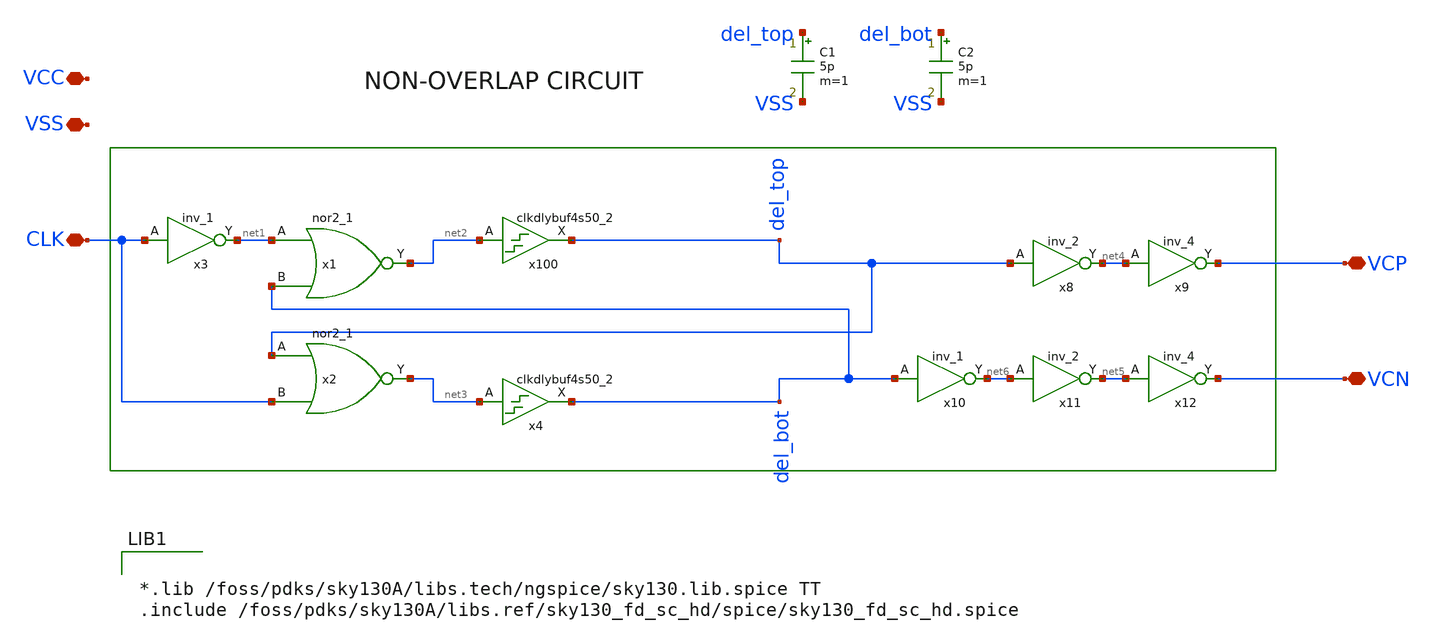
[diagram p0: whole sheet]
** sch_path: xschem/NOL_v3p1.sch
**.subckt NOL_v3p1 CLK VCP VCN VCC VSS
*.iopin CLK
*.iopin VCP
*.iopin VCN
*.iopin VCC
*.iopin VSS
x3 CLK VSS VSS VCC VCC net1 sky130_fd_sc_hd__inv_1
x1 net1 del_bot VSS VSS VCC VCC net2 sky130_fd_sc_hd__nor2_1
x2 del_top CLK VSS VSS VCC VCC net3 sky130_fd_sc_hd__nor2_1
x8 del_top VSS VSS VCC VCC net4 sky130_fd_sc_hd__inv_2
x9 net4 VSS VSS VCC VCC VCP sky130_fd_sc_hd__inv_4
x10 del_bot VSS VSS VCC VCC net6 sky130_fd_sc_hd__inv_1
x11 net6 VSS VSS VCC VCC net5 sky130_fd_sc_hd__inv_2
x12 net5 VSS VSS VCC VCC VCN sky130_fd_sc_hd__inv_4
x100 net2 VSS VSS VCC VCC del_top sky130_fd_sc_hd__clkdlybuf4s50_2
x4 net3 VSS VSS VCC VCC del_bot sky130_fd_sc_hd__clkdlybuf4s50_2
C1 del_top VSS 5p m=1
C2 del_bot VSS 5p m=1
**** begin user architecture code


*.lib /foss/pdks/sky130A/libs.tech/ngspice/sky130.lib.spice TT
.include /foss/pdks/sky130A/libs.ref/sky130_fd_sc_hd/spice/sky130_fd_sc_hd.spice


**** end user architecture code
**.ends
.end
